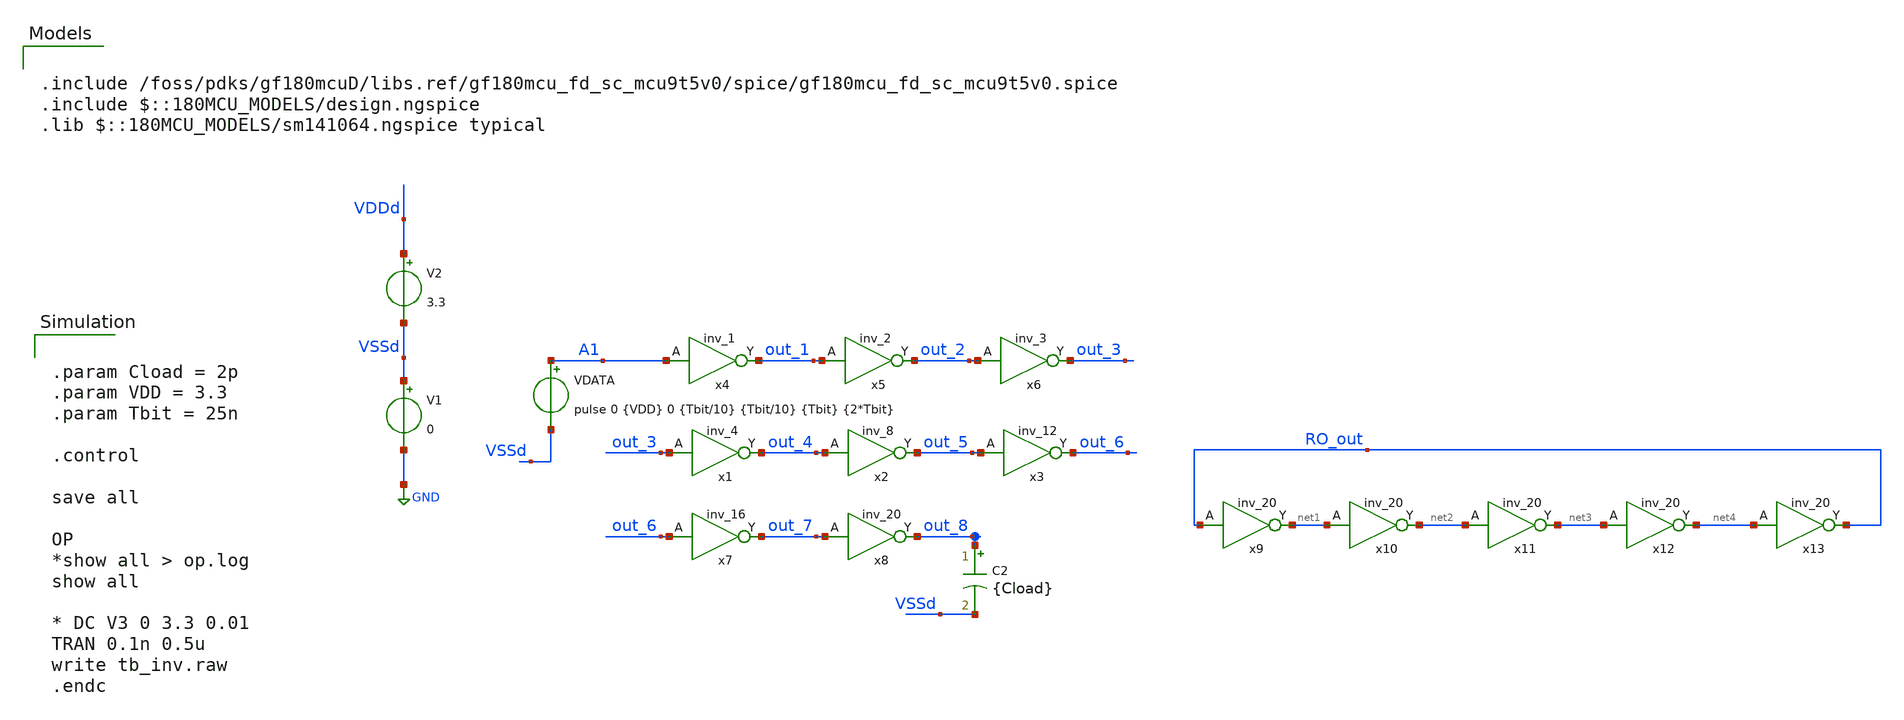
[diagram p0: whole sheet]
** sch_path: tb_digital_cells/tb_inv.sch
**.subckt tb_inv
V1 VSSd GND 0
V2 VDDd VSSd 3.3
VDATA A1 VSSd pulse 0 {VDD} 0 {Tbit/10} {Tbit/10} {Tbit} {2*Tbit}
x4 A1 out_1 VDDd VDDd VSSd VSSd gf180mcu_fd_sc_mcu9t5v0__inv_1
x5 out_1 out_2 VDDd VDDd VSSd VSSd gf180mcu_fd_sc_mcu9t5v0__inv_2
x6 out_2 out_3 VDDd VDDd VSSd VSSd gf180mcu_fd_sc_mcu9t5v0__inv_3
x1 out_3 out_4 VDDd VDDd VSSd VSSd gf180mcu_fd_sc_mcu9t5v0__inv_4
x2 out_4 out_5 VDDd VDDd VSSd VSSd gf180mcu_fd_sc_mcu9t5v0__inv_8
x3 out_5 out_6 VDDd VDDd VSSd VSSd gf180mcu_fd_sc_mcu9t5v0__inv_12
C2 out_8 VSSd {Cload} m=1
x8 out_7 out_8 VDDd VDDd VSSd VSSd gf180mcu_fd_sc_mcu9t5v0__inv_20
x7 out_6 out_7 VDDd VDDd VSSd VSSd gf180mcu_fd_sc_mcu9t5v0__inv_16
x9 RO_out net1 VDDd VDDd VSSd VSSd gf180mcu_fd_sc_mcu9t5v0__inv_20
x10 net1 net2 VDDd VDDd VSSd VSSd gf180mcu_fd_sc_mcu9t5v0__inv_20
x11 net2 net3 VDDd VDDd VSSd VSSd gf180mcu_fd_sc_mcu9t5v0__inv_20
x12 net3 net4 VDDd VDDd VSSd VSSd gf180mcu_fd_sc_mcu9t5v0__inv_20
x13 net4 RO_out VDDd VDDd VSSd VSSd gf180mcu_fd_sc_mcu9t5v0__inv_20
**** begin user architecture code


.param Cload = 2p
.param VDD = 3.3
.param Tbit = 25n

.control

save all

OP
*show all > op.log
show all

* DC V3 0 3.3 0.01
TRAN 0.1n 0.5u
write tb_inv.raw
.endc



.include /foss/pdks/gf180mcuD/libs.ref/gf180mcu_fd_sc_mcu9t5v0/spice/gf180mcu_fd_sc_mcu9t5v0.spice
.include $::180MCU_MODELS/design.ngspice
.lib $::180MCU_MODELS/sm141064.ngspice typical

**** end user architecture code
**.ends
.GLOBAL GND
.end
